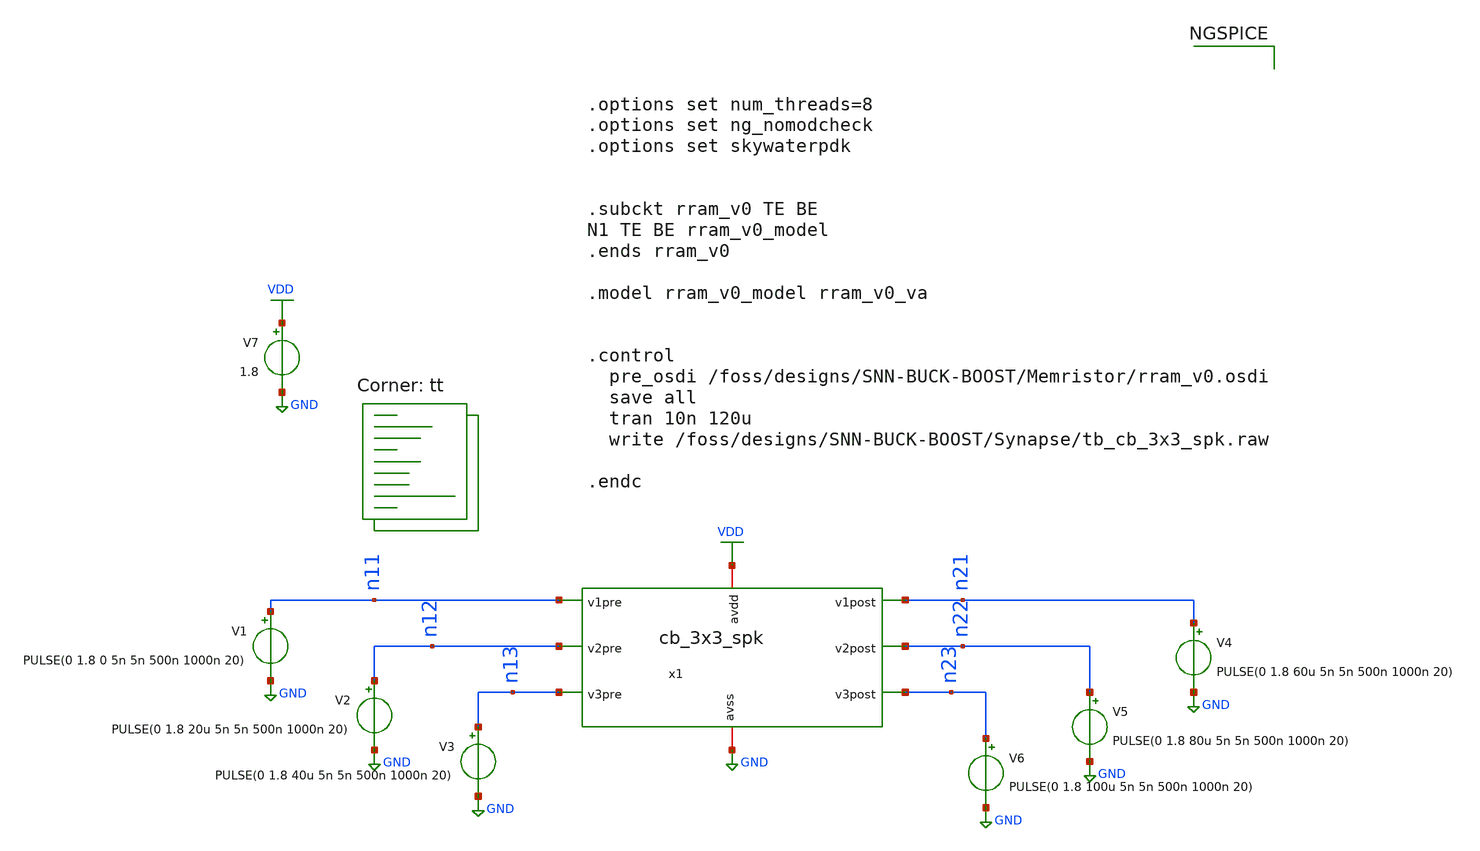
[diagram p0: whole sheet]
** sch_path: Synapse/tb_cb_3x3_spk.sch
**.subckt tb_cb_3x3_spk
x1 VDD GND n21 n11 n22 n12 n23 n13 cb_3x3_spk
V1 n11 GND PULSE(0 1.8 0 5n 5n 500n 1000n 20)
V2 n12 GND PULSE(0 1.8 20u 5n 5n 500n 1000n 20)
V3 n13 GND PULSE(0 1.8 40u 5n 5n 500n 1000n 20)
V4 n21 GND PULSE(0 1.8 60u 5n 5n 500n 1000n 20)
V5 n22 GND PULSE(0 1.8 80u 5n 5n 500n 1000n 20)
V6 n23 GND PULSE(0 1.8 100u 5n 5n 500n 1000n 20)
V7 VDD GND 1.8
**** begin user architecture code
.lib $::SKYWATER_MODELS/sky130.lib.spice tt



.options set num_threads=8
.options set ng_nomodcheck
.options set skywaterpdk


.subckt rram_v0 TE BE
N1 TE BE rram_v0_model
.ends rram_v0

.model rram_v0_model rram_v0_va


.control
  pre_osdi /foss/designs/SNN-BUCK-BOOST/Memristor/rram_v0.osdi
  save all
  tran 10n 120u
  write /foss/designs/SNN-BUCK-BOOST/Synapse/tb_cb_3x3_spk.raw

.endc



**** end user architecture code
**.ends

* expanding   symbol:  cb_3x3_spk.sym # of pins=8
** sym_path: Synapse/cb_3x3_spk.sym
** sch_path: Synapse/cb_3x3_spk.sch
.subckt cb_3x3_spk avdd avss v1post v1pre v2post v2pre v3post v3pre
*.iopin avdd
*.iopin avss
*.ipin v1post
*.ipin v2post
*.ipin v3post
*.ipin v1pre
*.ipin v2pre
*.ipin v3pre
XR13 net1 BE1 rram_v0
XM7 TE1 v1pre avss avss sky130_fd_pr__nfet_01v8 L=0.15 W=0.5 nf=1 ad='int((1 + 1)/2) * 0.5 / 1 * 0.29'
+ as='int((1 + 2)/2) * 0.5 / 1 * 0.29' pd='2*int((1 + 1)/2) * (0.5 / 1 + 0.29)' ps='2*int((1 + 2)/2) * (0.5 / 1 + 0.29)'
+ nrd='0.29 / 0.5 ' nrs='0.29 / 0.5 ' sa=0 sb=0 sd=0 mult=1 m=1
XM8 TE2 v2pre avss avss sky130_fd_pr__nfet_01v8 L=0.15 W=0.5 nf=1 ad='int((1 + 1)/2) * 0.5 / 1 * 0.29'
+ as='int((1 + 2)/2) * 0.5 / 1 * 0.29' pd='2*int((1 + 1)/2) * (0.5 / 1 + 0.29)' ps='2*int((1 + 2)/2) * (0.5 / 1 + 0.29)'
+ nrd='0.29 / 0.5 ' nrs='0.29 / 0.5 ' sa=0 sb=0 sd=0 mult=1 m=1
XM9 TE3 v3pre avss avss sky130_fd_pr__nfet_01v8 L=0.15 W=0.5 nf=1 ad='int((1 + 1)/2) * 0.5 / 1 * 0.29'
+ as='int((1 + 2)/2) * 0.5 / 1 * 0.29' pd='2*int((1 + 1)/2) * (0.5 / 1 + 0.29)' ps='2*int((1 + 2)/2) * (0.5 / 1 + 0.29)'
+ nrd='0.29 / 0.5 ' nrs='0.29 / 0.5 ' sa=0 sb=0 sd=0 mult=1 m=1
XM10 BE1 v1post avss avss sky130_fd_pr__nfet_01v8 L=0.15 W=0.5 nf=1 ad='int((1 + 1)/2) * 0.5 / 1 * 0.29'
+ as='int((1 + 2)/2) * 0.5 / 1 * 0.29' pd='2*int((1 + 1)/2) * (0.5 / 1 + 0.29)' ps='2*int((1 + 2)/2) * (0.5 / 1 + 0.29)'
+ nrd='0.29 / 0.5 ' nrs='0.29 / 0.5 ' sa=0 sb=0 sd=0 mult=1 m=1
XM11 BE2 v2post avss avss sky130_fd_pr__nfet_01v8 L=0.15 W=0.5 nf=1 ad='int((1 + 1)/2) * 0.5 / 1 * 0.29'
+ as='int((1 + 2)/2) * 0.5 / 1 * 0.29' pd='2*int((1 + 1)/2) * (0.5 / 1 + 0.29)' ps='2*int((1 + 2)/2) * (0.5 / 1 + 0.29)'
+ nrd='0.29 / 0.5 ' nrs='0.29 / 0.5 ' sa=0 sb=0 sd=0 mult=1 m=1
XM12 BE3 v3post avss avss sky130_fd_pr__nfet_01v8 L=0.15 W=0.5 nf=1 ad='int((1 + 1)/2) * 0.5 / 1 * 0.29'
+ as='int((1 + 2)/2) * 0.5 / 1 * 0.29' pd='2*int((1 + 1)/2) * (0.5 / 1 + 0.29)' ps='2*int((1 + 2)/2) * (0.5 / 1 + 0.29)'
+ nrd='0.29 / 0.5 ' nrs='0.29 / 0.5 ' sa=0 sb=0 sd=0 mult=1 m=1
XM13 BE1 nv1pre vp_pre avdd sky130_fd_pr__pfet_01v8 L=0.15 W=1 nf=1 ad='int((nf+1)/2) * W/nf * 0.29'
+ as='int((nf+2)/2) * W/nf * 0.29' pd='2*int((nf+1)/2) * (W/nf + 0.29)' ps='2*int((nf+2)/2) * (W/nf + 0.29)'
+ nrd='0.29 / W' nrs='0.29 / W' sa=0 sb=0 sd=0 mult=1 m=1
XM1 BE2 nv2pre vp_pre avdd sky130_fd_pr__pfet_01v8 L=0.15 W=1 nf=1 ad='int((nf+1)/2) * W/nf * 0.29' as='int((nf+2)/2) * W/nf * 0.29'
+ pd='2*int((nf+1)/2) * (W/nf + 0.29)' ps='2*int((nf+2)/2) * (W/nf + 0.29)' nrd='0.29 / W' nrs='0.29 / W'
+ sa=0 sb=0 sd=0 mult=1 m=1
XM2 BE3 nv3pre vp_pre avdd sky130_fd_pr__pfet_01v8 L=0.15 W=1 nf=1 ad='int((nf+1)/2) * W/nf * 0.29' as='int((nf+2)/2) * W/nf * 0.29'
+ pd='2*int((nf+1)/2) * (W/nf + 0.29)' ps='2*int((nf+2)/2) * (W/nf + 0.29)' nrd='0.29 / W' nrs='0.29 / W'
+ sa=0 sb=0 sd=0 mult=1 m=1
XM3 TE1 nv1post vp_post avdd sky130_fd_pr__pfet_01v8 L=0.15 W=1 nf=1 ad='int((nf+1)/2) * W/nf * 0.29'
+ as='int((nf+2)/2) * W/nf * 0.29' pd='2*int((nf+1)/2) * (W/nf + 0.29)' ps='2*int((nf+2)/2) * (W/nf + 0.29)'
+ nrd='0.29 / W' nrs='0.29 / W' sa=0 sb=0 sd=0 mult=1 m=1
XM4 TE2 nv2post vp_post avdd sky130_fd_pr__pfet_01v8 L=0.15 W=1 nf=1 ad='int((nf+1)/2) * W/nf * 0.29'
+ as='int((nf+2)/2) * W/nf * 0.29' pd='2*int((nf+1)/2) * (W/nf + 0.29)' ps='2*int((nf+2)/2) * (W/nf + 0.29)'
+ nrd='0.29 / W' nrs='0.29 / W' sa=0 sb=0 sd=0 mult=1 m=1
XM5 TE3 nv3post vp_post avdd sky130_fd_pr__pfet_01v8 L=0.15 W=1 nf=1 ad='int((nf+1)/2) * W/nf * 0.29'
+ as='int((nf+2)/2) * W/nf * 0.29' pd='2*int((nf+1)/2) * (W/nf + 0.29)' ps='2*int((nf+2)/2) * (W/nf + 0.29)'
+ nrd='0.29 / W' nrs='0.29 / W' sa=0 sb=0 sd=0 mult=1 m=1
XM6 nv1post v1post avdd avdd sky130_fd_pr__pfet_01v8 L=0.15 W=1 nf=1 ad='int((nf+1)/2) * W/nf * 0.29'
+ as='int((nf+2)/2) * W/nf * 0.29' pd='2*int((nf+1)/2) * (W/nf + 0.29)' ps='2*int((nf+2)/2) * (W/nf + 0.29)'
+ nrd='0.29 / W' nrs='0.29 / W' sa=0 sb=0 sd=0 mult=1 m=1
XM14 nv1post v1post avss avss sky130_fd_pr__nfet_01v8 L=0.15 W=0.5 nf=1 ad='int((1 + 1)/2) * 0.5 / 1 * 0.29'
+ as='int((1 + 2)/2) * 0.5 / 1 * 0.29' pd='2*int((1 + 1)/2) * (0.5 / 1 + 0.29)' ps='2*int((1 + 2)/2) * (0.5 / 1 + 0.29)'
+ nrd='0.29 / 0.5 ' nrs='0.29 / 0.5 ' sa=0 sb=0 sd=0 mult=1 m=1
XM15 nv2post v2post avdd avdd sky130_fd_pr__pfet_01v8 L=0.15 W=1 nf=1 ad='int((nf+1)/2) * W/nf * 0.29'
+ as='int((nf+2)/2) * W/nf * 0.29' pd='2*int((nf+1)/2) * (W/nf + 0.29)' ps='2*int((nf+2)/2) * (W/nf + 0.29)'
+ nrd='0.29 / W' nrs='0.29 / W' sa=0 sb=0 sd=0 mult=1 m=1
XM16 nv2post v2post avss avss sky130_fd_pr__nfet_01v8 L=0.15 W=0.5 nf=1 ad='int((1 + 1)/2) * 0.5 / 1 * 0.29'
+ as='int((1 + 2)/2) * 0.5 / 1 * 0.29' pd='2*int((1 + 1)/2) * (0.5 / 1 + 0.29)' ps='2*int((1 + 2)/2) * (0.5 / 1 + 0.29)'
+ nrd='0.29 / 0.5 ' nrs='0.29 / 0.5 ' sa=0 sb=0 sd=0 mult=1 m=1
XM17 nv3post v3post avdd avdd sky130_fd_pr__pfet_01v8 L=0.15 W=1 nf=1 ad='int((nf+1)/2) * W/nf * 0.29'
+ as='int((nf+2)/2) * W/nf * 0.29' pd='2*int((nf+1)/2) * (W/nf + 0.29)' ps='2*int((nf+2)/2) * (W/nf + 0.29)'
+ nrd='0.29 / W' nrs='0.29 / W' sa=0 sb=0 sd=0 mult=1 m=1
XM18 nv3post v3post avss avss sky130_fd_pr__nfet_01v8 L=0.15 W=0.5 nf=1 ad='int((1 + 1)/2) * 0.5 / 1 * 0.29'
+ as='int((1 + 2)/2) * 0.5 / 1 * 0.29' pd='2*int((1 + 1)/2) * (0.5 / 1 + 0.29)' ps='2*int((1 + 2)/2) * (0.5 / 1 + 0.29)'
+ nrd='0.29 / 0.5 ' nrs='0.29 / 0.5 ' sa=0 sb=0 sd=0 mult=1 m=1
XM19 nv1pre v1pre avdd avdd sky130_fd_pr__pfet_01v8 L=0.15 W=1 nf=1 ad='int((nf+1)/2) * W/nf * 0.29'
+ as='int((nf+2)/2) * W/nf * 0.29' pd='2*int((nf+1)/2) * (W/nf + 0.29)' ps='2*int((nf+2)/2) * (W/nf + 0.29)'
+ nrd='0.29 / W' nrs='0.29 / W' sa=0 sb=0 sd=0 mult=1 m=1
XM20 nv1pre v1pre avss avss sky130_fd_pr__nfet_01v8 L=0.15 W=0.5 nf=1 ad='int((1 + 1)/2) * 0.5 / 1 * 0.29'
+ as='int((1 + 2)/2) * 0.5 / 1 * 0.29' pd='2*int((1 + 1)/2) * (0.5 / 1 + 0.29)' ps='2*int((1 + 2)/2) * (0.5 / 1 + 0.29)'
+ nrd='0.29 / 0.5 ' nrs='0.29 / 0.5 ' sa=0 sb=0 sd=0 mult=1 m=1
XM21 nv2pre v2pre avdd avdd sky130_fd_pr__pfet_01v8 L=0.15 W=1 nf=1 ad='int((nf+1)/2) * W/nf * 0.29'
+ as='int((nf+2)/2) * W/nf * 0.29' pd='2*int((nf+1)/2) * (W/nf + 0.29)' ps='2*int((nf+2)/2) * (W/nf + 0.29)'
+ nrd='0.29 / W' nrs='0.29 / W' sa=0 sb=0 sd=0 mult=1 m=1
XM22 nv2pre v2pre avss avss sky130_fd_pr__nfet_01v8 L=0.15 W=0.5 nf=1 ad='int((1 + 1)/2) * 0.5 / 1 * 0.29'
+ as='int((1 + 2)/2) * 0.5 / 1 * 0.29' pd='2*int((1 + 1)/2) * (0.5 / 1 + 0.29)' ps='2*int((1 + 2)/2) * (0.5 / 1 + 0.29)'
+ nrd='0.29 / 0.5 ' nrs='0.29 / 0.5 ' sa=0 sb=0 sd=0 mult=1 m=1
XM23 nv3pre v3pre avdd avdd sky130_fd_pr__pfet_01v8 L=0.15 W=1 nf=1 ad='int((nf+1)/2) * W/nf * 0.29'
+ as='int((nf+2)/2) * W/nf * 0.29' pd='2*int((nf+1)/2) * (W/nf + 0.29)' ps='2*int((nf+2)/2) * (W/nf + 0.29)'
+ nrd='0.29 / W' nrs='0.29 / W' sa=0 sb=0 sd=0 mult=1 m=1
XM24 nv3pre v3pre avss avss sky130_fd_pr__nfet_01v8 L=0.15 W=0.5 nf=1 ad='int((1 + 1)/2) * 0.5 / 1 * 0.29'
+ as='int((1 + 2)/2) * 0.5 / 1 * 0.29' pd='2*int((1 + 1)/2) * (0.5 / 1 + 0.29)' ps='2*int((1 + 2)/2) * (0.5 / 1 + 0.29)'
+ nrd='0.29 / 0.5 ' nrs='0.29 / 0.5 ' sa=0 sb=0 sd=0 mult=1 m=1
**** begin user architecture code


*.save v(TE1) v(TE2) v(TE3)
*.save v(BE1) v(BE2) v(TE3)
*.save all


**** end user architecture code
vam13 net1 TE3 0
.save i(vam13)
XR23 net2 BE2 rram_v0
vam23 net2 TE3 0
.save i(vam23)
XR33 net3 BE3 rram_v0
vam33 net3 TE3 0
.save i(vam33)
XR32 net4 BE3 rram_v0
vam32 net4 TE2 0
.save i(vam32)
XR22 net5 BE2 rram_v0
vam22 net5 TE2 0
.save i(vam22)
XR12 net6 BE1 rram_v0
vam12 net6 TE2 0
.save i(vam12)
XR11 net7 BE1 rram_v0
vam11 net7 TE1 0
.save i(vam11)
XR21 net8 BE2 rram_v0
vam21 net8 TE1 0
.save i(vam21)
XR31 net9 BE3 rram_v0
vam31 net9 TE1 0
.save i(vam31)
XM25 vp_post vp_post avdd avdd sky130_fd_pr__pfet_01v8 L=0.15 W=3 nf=1 ad='int((nf+1)/2) * W/nf * 0.29'
+ as='int((nf+2)/2) * W/nf * 0.29' pd='2*int((nf+1)/2) * (W/nf + 0.29)' ps='2*int((nf+2)/2) * (W/nf + 0.29)'
+ nrd='0.29 / W' nrs='0.29 / W' sa=0 sb=0 sd=0 mult=1 m=1
XM26 vp_pre vp_pre avdd avdd sky130_fd_pr__pfet_01v8 L=0.15 W=3 nf=1 ad='int((nf+1)/2) * W/nf * 0.29'
+ as='int((nf+2)/2) * W/nf * 0.29' pd='2*int((nf+1)/2) * (W/nf + 0.29)' ps='2*int((nf+2)/2) * (W/nf + 0.29)'
+ nrd='0.29 / W' nrs='0.29 / W' sa=0 sb=0 sd=0 mult=1 m=1
.ends

.GLOBAL GND
.GLOBAL VDD
.end
